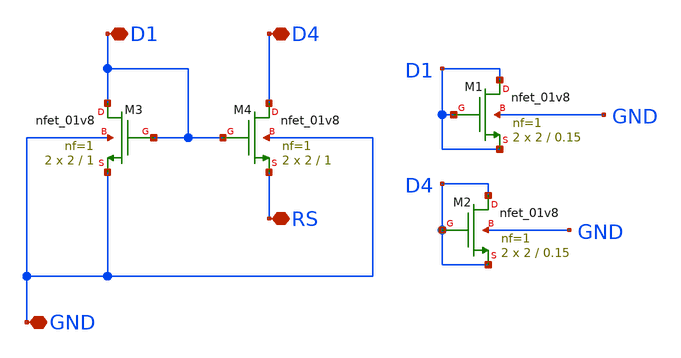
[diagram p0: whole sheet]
** sch_path: opamp/mag/nmosdp.sch
**.subckt nmosdp D1 D4 GND RS
*.iopin D1
*.iopin D4
*.iopin GND
*.iopin RS
XM3 D1 D1 GND GND sky130_fd_pr__nfet_01v8 L=1 W=2 nf=1 ad='int((nf+1)/2) * W/nf * 0.29' as='int((nf+2)/2) * W/nf * 0.29'
+ pd='2*int((nf+1)/2) * (W/nf + 0.29)' ps='2*int((nf+2)/2) * (W/nf + 0.29)' nrd='0.29 / W' nrs='0.29 / W'
+ sa=0 sb=0 sd=0 mult=2 m=2
XM4 D4 D1 RS GND sky130_fd_pr__nfet_01v8 L=1 W=2 nf=1 ad='int((nf+1)/2) * W/nf * 0.29' as='int((nf+2)/2) * W/nf * 0.29'
+ pd='2*int((nf+1)/2) * (W/nf + 0.29)' ps='2*int((nf+2)/2) * (W/nf + 0.29)' nrd='0.29 / W' nrs='0.29 / W'
+ sa=0 sb=0 sd=0 mult=2 m=2
XM1 D1 D1 D1 GND sky130_fd_pr__nfet_01v8 L=0.15 W=2 nf=1 ad='int((nf+1)/2) * W/nf * 0.29' as='int((nf+2)/2) * W/nf * 0.29'
+ pd='2*int((nf+1)/2) * (W/nf + 0.29)' ps='2*int((nf+2)/2) * (W/nf + 0.29)' nrd='0.29 / W' nrs='0.29 / W'
+ sa=0 sb=0 sd=0 mult=2 m=2
XM2 D4 D4 D4 GND sky130_fd_pr__nfet_01v8 L=0.15 W=2 nf=1 ad='int((nf+1)/2) * W/nf * 0.29' as='int((nf+2)/2) * W/nf * 0.29'
+ pd='2*int((nf+1)/2) * (W/nf + 0.29)' ps='2*int((nf+2)/2) * (W/nf + 0.29)' nrd='0.29 / W' nrs='0.29 / W'
+ sa=0 sb=0 sd=0 mult=2 m=2
**.ends
.end
